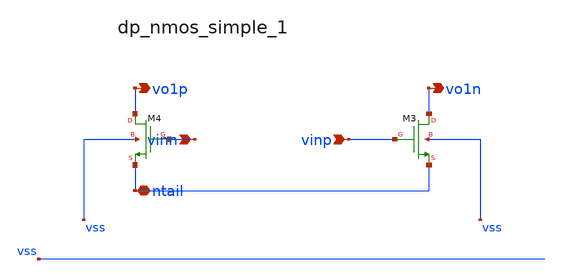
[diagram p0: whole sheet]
** sch_path: analog-db/raw/amp_031_srmc_core_cmfb/hier/blocks/dp_nmos_simple_1.sch
**.subckt dp_nmos_simple_1 vinn vinp ntail vo1p vo1n
*.ipin vinn
*.ipin vinp
*.iopin ntail
*.opin vo1p
*.opin vo1n
XM3 vo1n vinp ntail vss sg13_lv_nmos w=x_dut_xm3_w l=x_dut_xm3_l ng=1 m=x_dut_xm3_m
XM4 vo1p vinn ntail vss sg13_lv_nmos w=x_dut_xm4_w l=x_dut_xm4_l ng=1 m=x_dut_xm4_m
**.ends
.end
